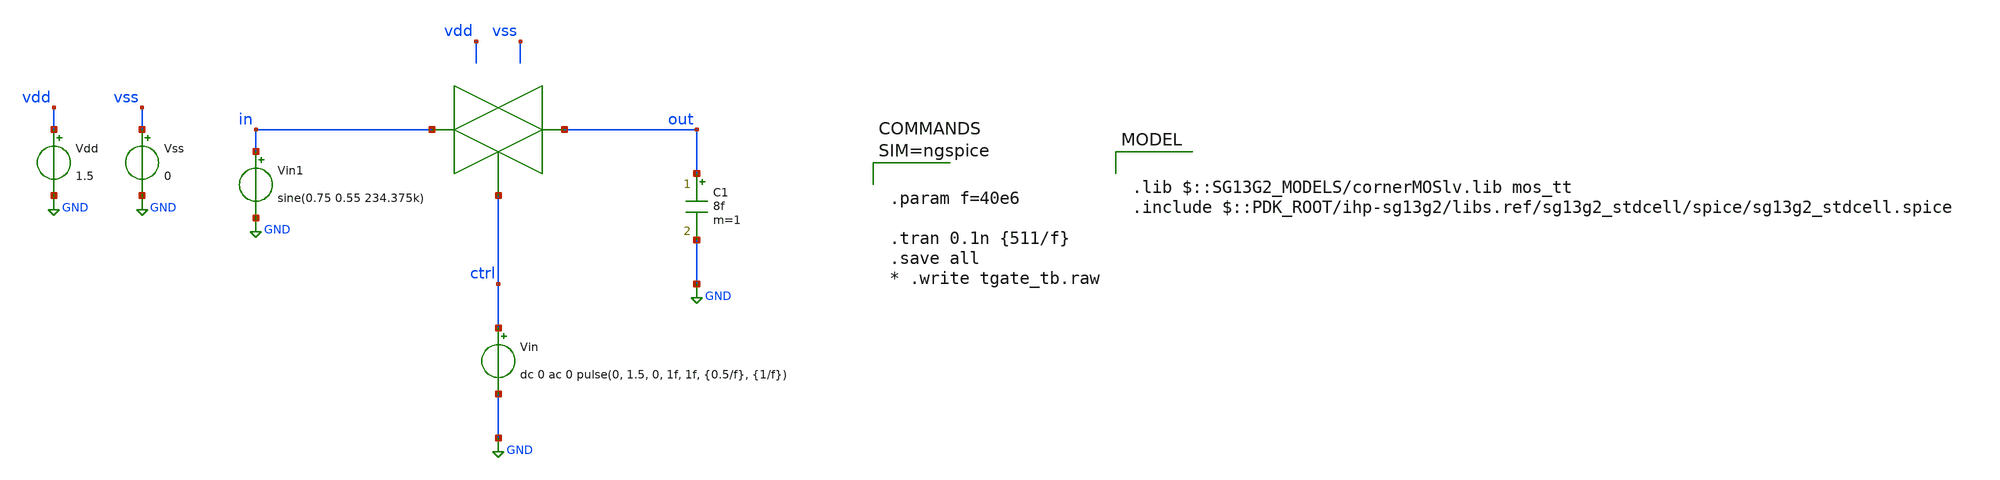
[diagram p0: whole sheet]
** sch_path: designs/tgate/tgate_tb.sch
**.subckt tgate_tb
Vin ctrl GND dc 0 ac 0 pulse(0, 1.5, 0, 1f, 1f, {0.5/f}, {1/f})
Vdd vdd GND 1.5
Vss vss GND 0
C1 out GND 8f m=1
Vin1 in GND sine(0.75 0.55 234.375k)
**** begin user architecture code



.param f=40e6

.tran 0.1n {511/f}
.save all
* .write tgate_tb.raw




.lib $::SG13G2_MODELS/cornerMOSlv.lib mos_tt
.include $::PDK_ROOT/ihp-sg13g2/libs.ref/sg13g2_stdcell/spice/sg13g2_stdcell.spice

**** end user architecture code
**.ends
.GLOBAL GND
.end
